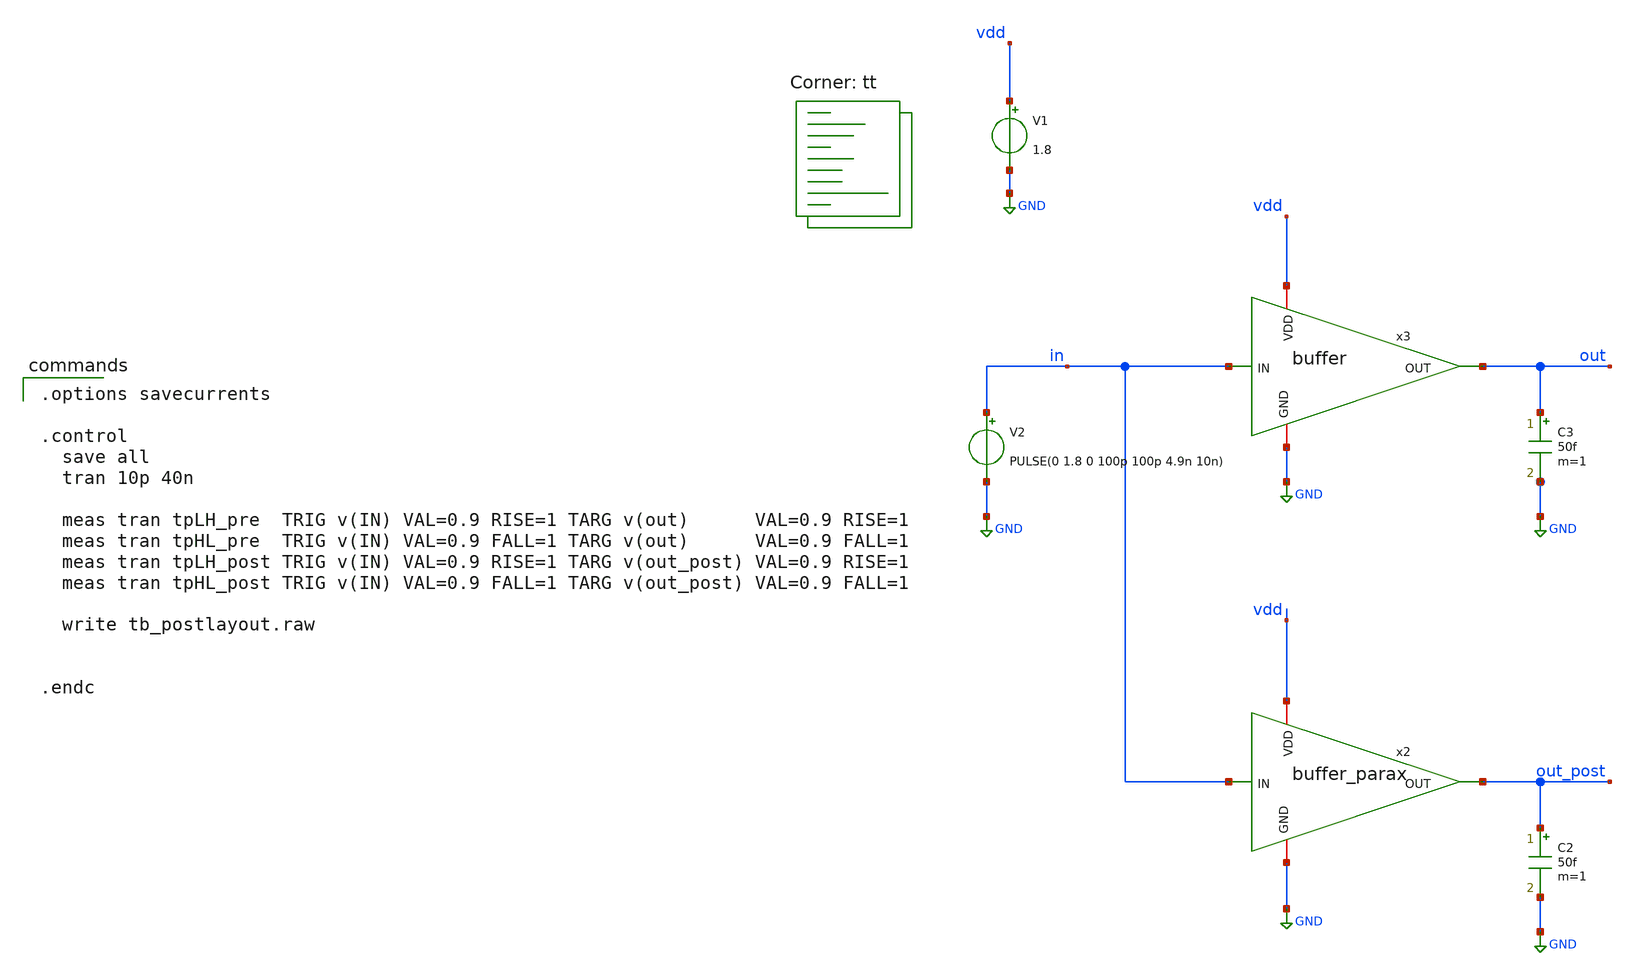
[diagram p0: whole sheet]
** sch_path: 03_magic_layout/soluzioni/lab03/xschem/tb_postlayout.sch
**.subckt tb_postlayout
V1 vdd GND 1.8
V2 in GND PULSE(0 1.8 0 100p 100p 4.9n 10n)
x2 vdd GND out_post in buffer_parax
C2 out_post GND 50f m=1
C3 out GND 50f m=1
x3 vdd GND out in buffer
**** begin user architecture code
.lib $::SKYWATER_MODELS/sky130.lib.spice tt

.options savecurrents

.control
  save all
  tran 10p 40n

  meas tran tpLH_pre  TRIG v(IN) VAL=0.9 RISE=1 TARG v(out)      VAL=0.9 RISE=1
  meas tran tpHL_pre  TRIG v(IN) VAL=0.9 FALL=1 TARG v(out)      VAL=0.9 FALL=1
  meas tran tpLH_post TRIG v(IN) VAL=0.9 RISE=1 TARG v(out_post) VAL=0.9 RISE=1
  meas tran tpHL_post TRIG v(IN) VAL=0.9 FALL=1 TARG v(out_post) VAL=0.9 FALL=1

  write tb_postlayout.raw


.endc

**** end user architecture code
**.ends
.GLOBAL GND
.end
